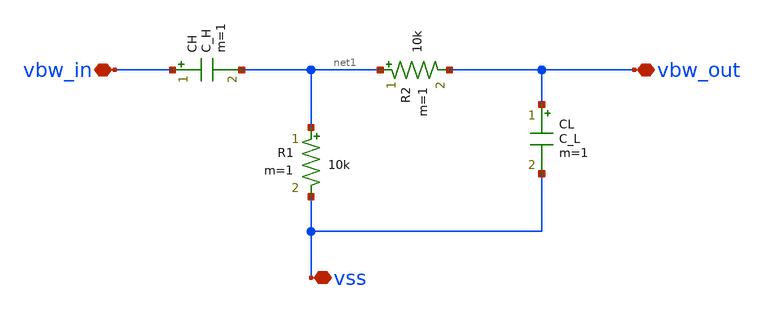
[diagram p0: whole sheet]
** sch_path: Synapse/bpfilter.sch
**.subckt bpfilter vbw_in vbw_out vss
*.iopin vbw_in
*.iopin vbw_out
*.iopin vss
R1 net1 vss 10k m=1
R2 net1 vbw_out 10k m=1
CL vbw_out vss C_L m=1
CH vbw_in net1 C_H m=1
**.ends
.end
